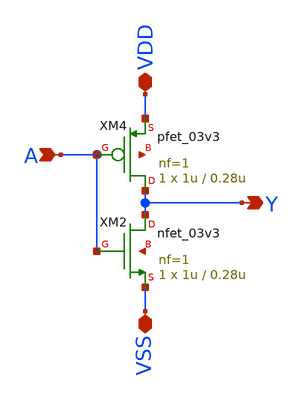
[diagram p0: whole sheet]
** sch_path: team_src/xschem/NOT_v1.sch
**.subckt NOT_v1 VSS VDD A Y
*.iopin VSS
*.iopin VDD
*.ipin A
*.opin Y
XM2 Y A VSS net1 nfet_03v3 L=0.28u W=1u nf=1 ad='int((nf+1)/2) * W/nf * 0.18u' as='int((nf+2)/2) * W/nf * 0.18u'
+ pd='2*int((nf+1)/2) * (W/nf + 0.18u)' ps='2*int((nf+2)/2) * (W/nf + 0.18u)' nrd='0.18u / W' nrs='0.18u / W'
+ sa=0 sb=0 sd=0 m=1
XM4 Y A VDD net2 pfet_03v3 L=0.28u W=1u nf=1 ad='int((nf+1)/2) * W/nf * 0.18u' as='int((nf+2)/2) * W/nf * 0.18u'
+ pd='2*int((nf+1)/2) * (W/nf + 0.18u)' ps='2*int((nf+2)/2) * (W/nf + 0.18u)' nrd='0.18u / W' nrs='0.18u / W'
+ sa=0 sb=0 sd=0 m=1
**.ends
.end
